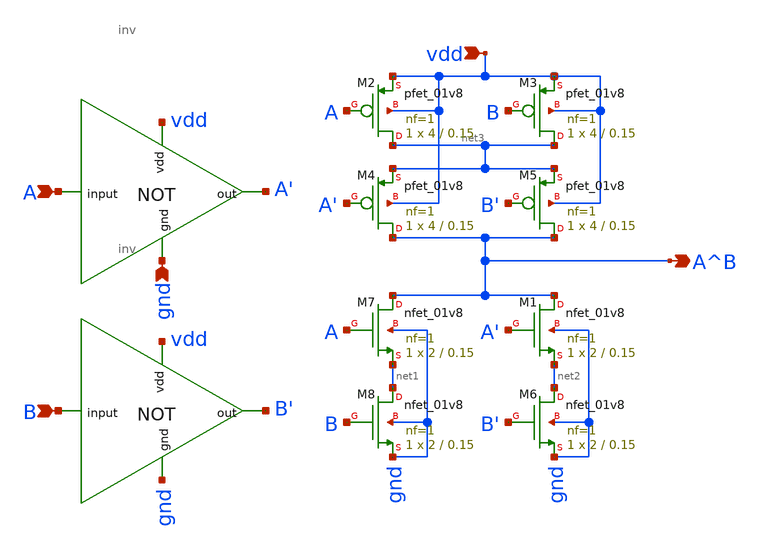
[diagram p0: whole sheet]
** sch_path: schematics/xor.sch
**.subckt xor vdd A B gnd A^B
*.ipin vdd
*.ipin A
*.ipin B
*.ipin gnd
*.opin A^B
XM1 A^B A' net2 gnd sky130_fd_pr__nfet_01v8 L=0.15 W=2 nf=1 ad='int((1 + 1)/2) * 2 / 1 * 0.29' as='int((1
+ + 2)/2) * 2 / 1 * 0.29' pd='2*int((1 + 1)/2) * (2 / 1 + 0.29)' ps='2*int((1 + 2)/2) * (2 / 1 + 0.29)' nrd='0.29
+ / 2 ' nrs='0.29 / 2 ' sa=0 sb=0 sd=0 mult=1 m=1
XM2 net3 A vdd vdd sky130_fd_pr__pfet_01v8 L=0.15 W=4 nf=1 ad='int((1 + 1)/2) * 4 / 1 * 0.29' as='int((1
+ + 2)/2) * 4 / 1 * 0.29' pd='2*int((1 + 1)/2) * (4 / 1 + 0.29)' ps='2*int((1 + 2)/2) * (4 / 1 + 0.29)' nrd='0.29
+ / 4 ' nrs='0.29 / 4 ' sa=0 sb=0 sd=0 mult=1 m=1
XM3 net3 B vdd vdd sky130_fd_pr__pfet_01v8 L=0.15 W=4 nf=1 ad='int((1 + 1)/2) * 4 / 1 * 0.29' as='int((1
+ + 2)/2) * 4 / 1 * 0.29' pd='2*int((1 + 1)/2) * (4 / 1 + 0.29)' ps='2*int((1 + 2)/2) * (4 / 1 + 0.29)' nrd='0.29
+ / 4 ' nrs='0.29 / 4 ' sa=0 sb=0 sd=0 mult=1 m=1
XM4 A^B A' net3 vdd sky130_fd_pr__pfet_01v8 L=0.15 W=4 nf=1 ad='int((1 + 1)/2) * 4 / 1 * 0.29' as='int((1 + 2)/2) * 4 / 1 * 0.29'
+ pd='2*int((1 + 1)/2) * (4 / 1 + 0.29)' ps='2*int((1 + 2)/2) * (4 / 1 + 0.29)' nrd='0.29 / 4 ' nrs='0.29 / 4 '
+ sa=0 sb=0 sd=0 mult=1 m=1
XM5 A^B B' net3 vdd sky130_fd_pr__pfet_01v8 L=0.15 W=4 nf=1 ad='int((1 + 1)/2) * 4 / 1 * 0.29' as='int((1
+ + 2)/2) * 4 / 1 * 0.29' pd='2*int((1 + 1)/2) * (4 / 1 + 0.29)' ps='2*int((1 + 2)/2) * (4 / 1 + 0.29)' nrd='0.29
+ / 4 ' nrs='0.29 / 4 ' sa=0 sb=0 sd=0 mult=1 m=1
XM6 net2 B' gnd gnd sky130_fd_pr__nfet_01v8 L=0.15 W=2 nf=1 ad='int((1 + 1)/2) * 2 / 1 * 0.29' as='int((1 + 2)/2) * 2 / 1 * 0.29'
+ pd='2*int((1 + 1)/2) * (2 / 1 + 0.29)' ps='2*int((1 + 2)/2) * (2 / 1 + 0.29)' nrd='0.29 / 2 ' nrs='0.29 / 2 '
+ sa=0 sb=0 sd=0 mult=1 m=1
XM7 A^B A net1 gnd sky130_fd_pr__nfet_01v8 L=0.15 W=2 nf=1 ad='int((1 + 1)/2) * 2 / 1 * 0.29' as='int((1 + 2)/2) * 2 / 1 * 0.29'
+ pd='2*int((1 + 1)/2) * (2 / 1 + 0.29)' ps='2*int((1 + 2)/2) * (2 / 1 + 0.29)' nrd='0.29 / 2 ' nrs='0.29 / 2 '
+ sa=0 sb=0 sd=0 mult=1 m=1
XM8 net1 B gnd gnd sky130_fd_pr__nfet_01v8 L=0.15 W=2 nf=1 ad='int((1 + 1)/2) * 2 / 1 * 0.29' as='int((1 + 2)/2) * 2 / 1 * 0.29'
+ pd='2*int((1 + 1)/2) * (2 / 1 + 0.29)' ps='2*int((1 + 2)/2) * (2 / 1 + 0.29)' nrd='0.29 / 2 ' nrs='0.29 / 2 '
+ sa=0 sb=0 sd=0 mult=1 m=1
x1 A' vdd A gnd inv
x2 B' vdd B gnd inv
**.ends
.end
